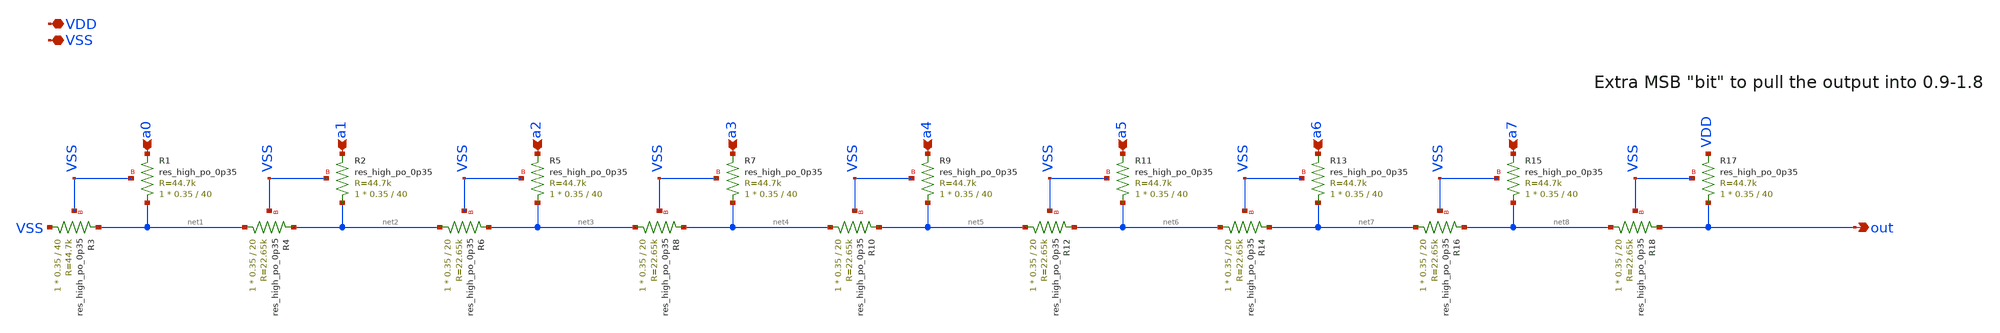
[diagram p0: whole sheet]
** sch_path: xschem/dac.sch
**.subckt dac VSS a0 a1 a2 a3 a4 a5 out a6 a7 VDD
*.iopin VSS
*.ipin a0
*.ipin a1
*.ipin a2
*.ipin a3
*.ipin a4
*.ipin a5
*.opin out
*.ipin a6
*.ipin a7
*.iopin VDD
XR1 net1 a0 VSS sky130_fd_pr__res_high_po_0p35 L=40 mult=1 m=1
XR3 VSS net1 VSS sky130_fd_pr__res_high_po_0p35 L=40 mult=1 m=1
XR2 net2 a1 VSS sky130_fd_pr__res_high_po_0p35 L=40 mult=1 m=1
XR4 net1 net2 VSS sky130_fd_pr__res_high_po_0p35 L=20 mult=1 m=1
XR5 net3 a2 VSS sky130_fd_pr__res_high_po_0p35 L=40 mult=1 m=1
XR6 net2 net3 VSS sky130_fd_pr__res_high_po_0p35 L=20 mult=1 m=1
XR7 net4 a3 VSS sky130_fd_pr__res_high_po_0p35 L=40 mult=1 m=1
XR8 net3 net4 VSS sky130_fd_pr__res_high_po_0p35 L=20 mult=1 m=1
XR9 net5 a4 VSS sky130_fd_pr__res_high_po_0p35 L=40 mult=1 m=1
XR10 net4 net5 VSS sky130_fd_pr__res_high_po_0p35 L=20 mult=1 m=1
XR11 net6 a5 VSS sky130_fd_pr__res_high_po_0p35 L=40 mult=1 m=1
XR12 net5 net6 VSS sky130_fd_pr__res_high_po_0p35 L=20 mult=1 m=1
XR13 net7 a6 VSS sky130_fd_pr__res_high_po_0p35 L=40 mult=1 m=1
XR14 net6 net7 VSS sky130_fd_pr__res_high_po_0p35 L=20 mult=1 m=1
XR15 net8 a7 VSS sky130_fd_pr__res_high_po_0p35 L=40 mult=1 m=1
XR16 net7 net8 VSS sky130_fd_pr__res_high_po_0p35 L=20 mult=1 m=1
XR17 out VDD VSS sky130_fd_pr__res_high_po_0p35 L=40 mult=1 m=1
XR18 net8 out VSS sky130_fd_pr__res_high_po_0p35 L=20 mult=1 m=1
**.ends
.end
